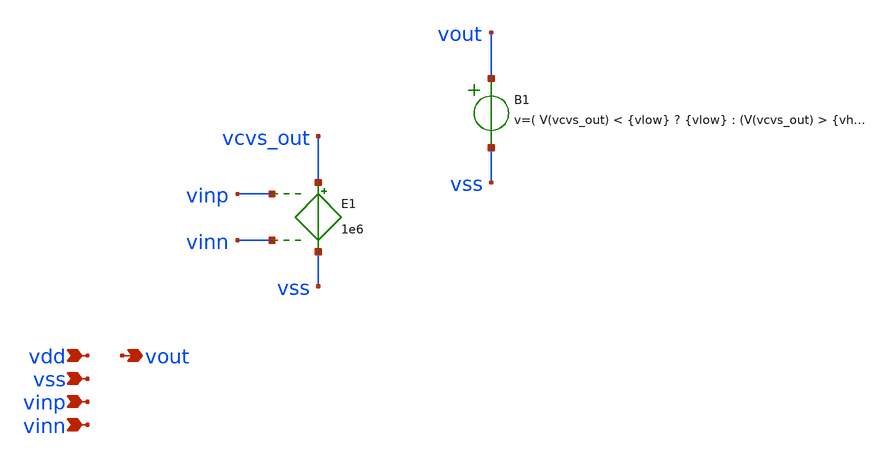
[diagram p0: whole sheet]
** sch_path: schematics/ideal_comp.sch
**.subckt ideal_comp vdd vout vss vinp vinn
*.ipin vdd
*.opin vout
*.ipin vss
*.ipin vinp
*.ipin vinn
E1 vcvs_out vss vinp vinn 1e6
B1 vout vss v=( V(vcvs_out) < {vlow} ? {vlow} : (V(vcvs_out) > {vhigh} ? {vhigh} : V(vcvs_out)))
**.ends
.end
